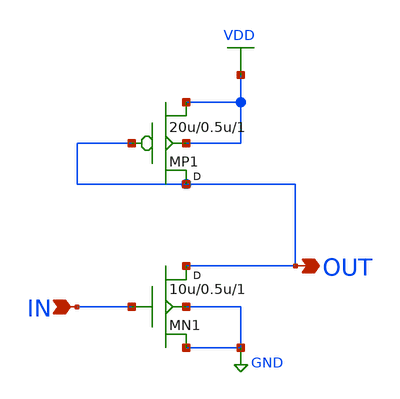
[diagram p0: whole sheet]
** sch_path: E3_238_Analog_VLSI_Circuits/07_Diode_Load_CS_Amplifier/cs_diode_load.sch
**.subckt cs_diode_load IN OUT
*.ipin IN
*.opin OUT
MP1 OUT OUT VDD VDD pmos w=20u l=0.5u m=1
MN1 OUT IN GND GND nmos w=10u l=0.5u m=1
**** begin user architecture code

.include /home/anirudh/Analog_VLSI_Projects/models/cmos_180nm.mod
VDD VDD 0 DC 1.8
VIN IN 0 DC 0.9 AC 1
CL OUT 0 1p

.control
  op
  print v(OUT)
  ac dec 20 1 1G
  plot db(v(OUT))
  plot phase(v(OUT))*180/pi
.endc


**** end user architecture code
**.ends
.GLOBAL VDD
.GLOBAL GND
.end
